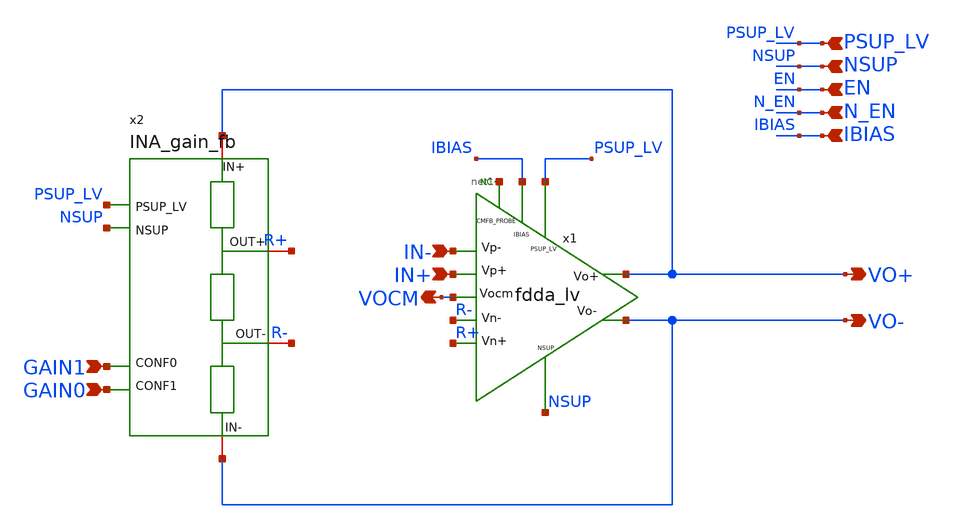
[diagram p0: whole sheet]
** sch_path: xschem/blocks/INA/INA.sch
**.subckt INA VO+ VO- IN+ IN- NSUP EN N_EN IBIAS PSUP_LV GAIN0 GAIN1 VOCM
*.opin VO+
*.opin VO-
*.ipin IN+
*.ipin IN-
*.ipin NSUP
*.ipin EN
*.ipin N_EN
*.ipin IBIAS
*.ipin PSUP_LV
*.ipin GAIN0
*.ipin GAIN1
*.opin VOCM
* noconn #net1
x1 PSUP_LV IN- R- R+ IN+ VO+ VO- IBIAS NSUP net1 VOCM fdda_lv
x2 VO+ R+ PSUP_LV NSUP GAIN0 GAIN1 R- VO- INA_gain_fb
**.ends
.end
